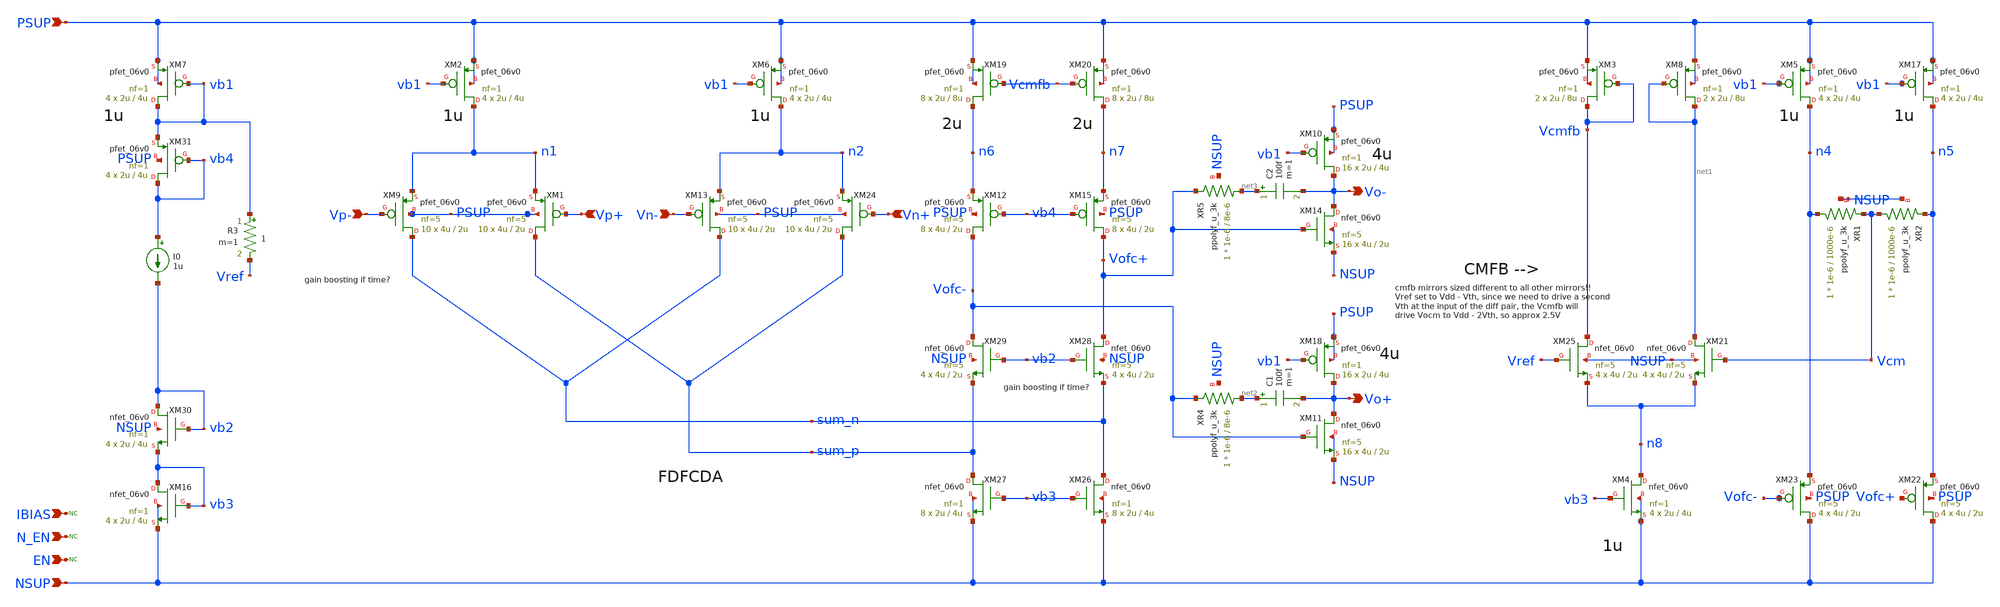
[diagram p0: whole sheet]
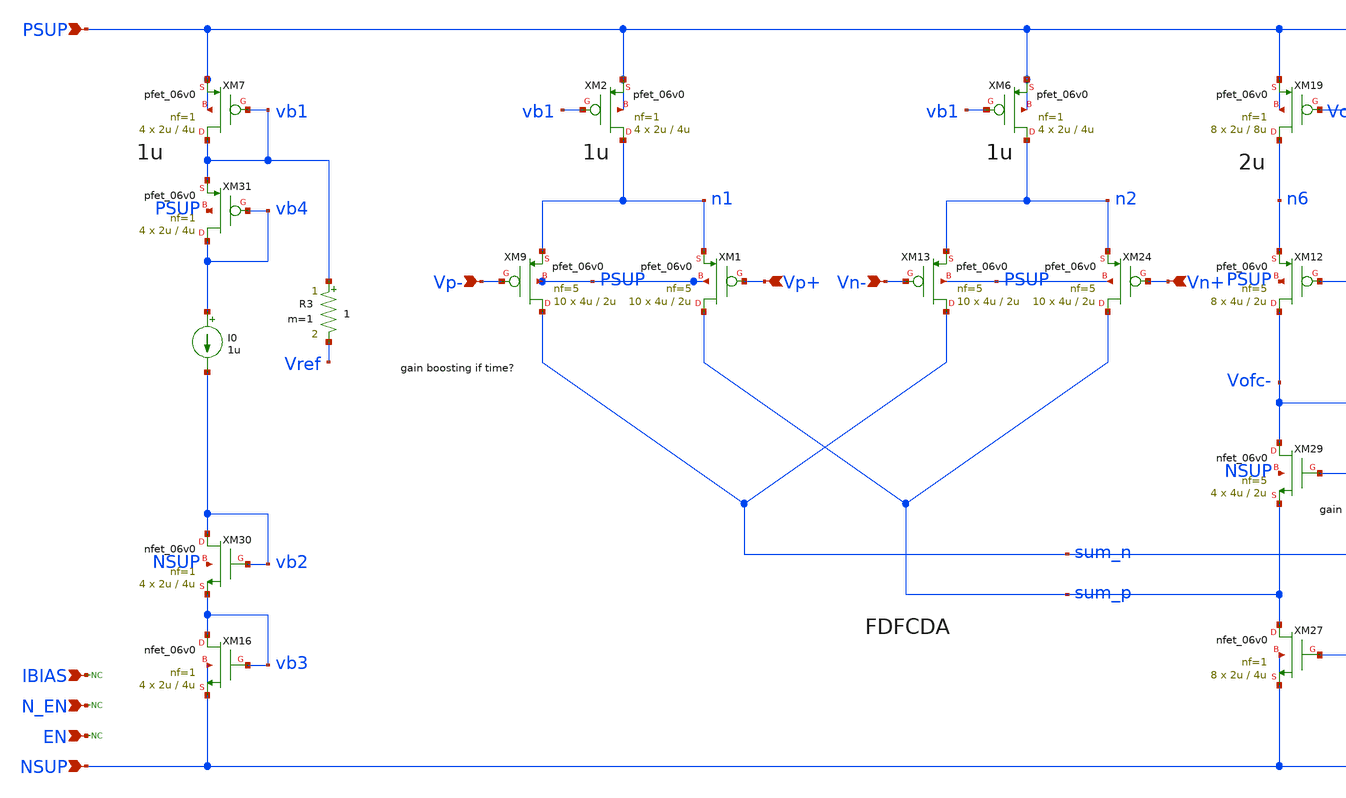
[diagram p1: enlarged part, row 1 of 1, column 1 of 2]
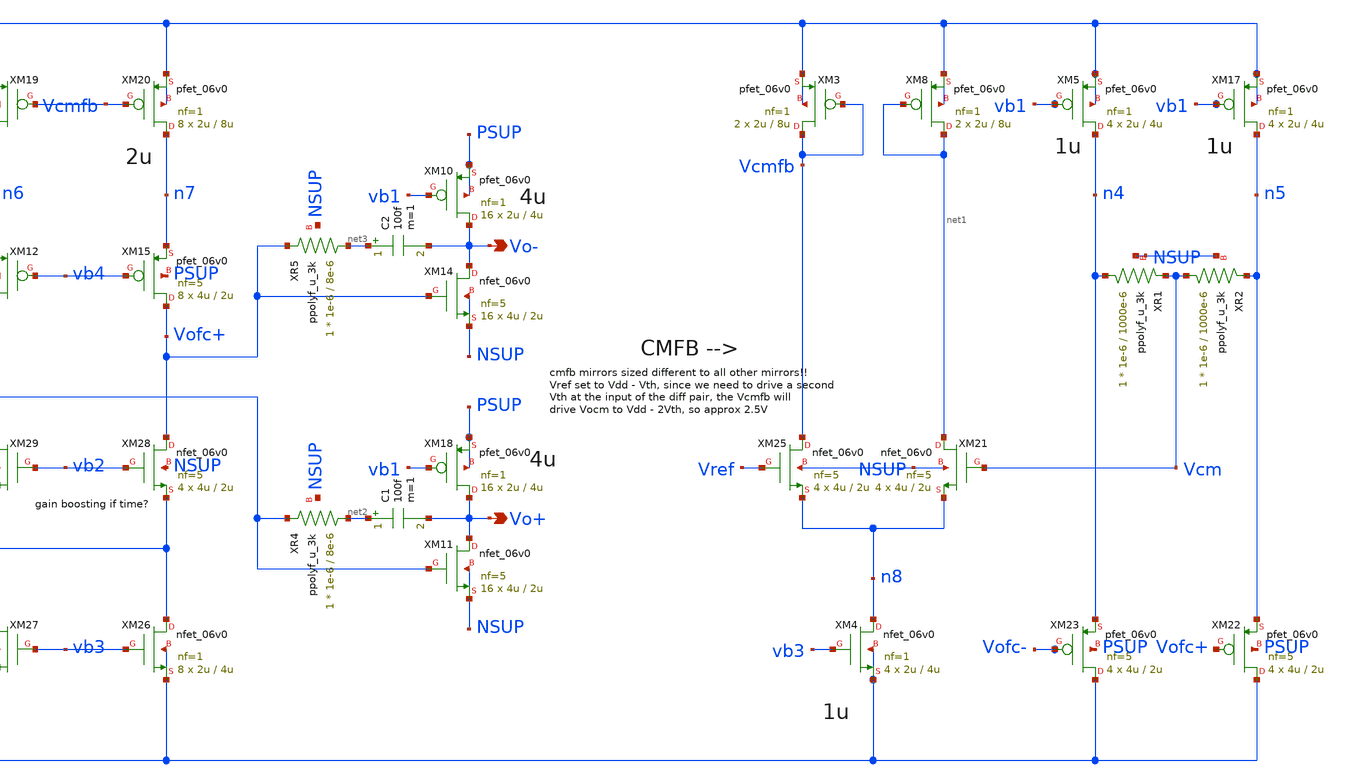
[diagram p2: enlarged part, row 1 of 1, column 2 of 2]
** sch_path: xschem/blocks/fdda/junk/fdda_most_recent.sch
**.subckt fdda_most_recent PSUP NSUP N_EN EN IBIAS Vp+ Vp- Vn+ Vn- Vo- Vo+
*.ipin PSUP
*.ipin NSUP
*.ipin N_EN
*.ipin EN
*.ipin IBIAS
*.ipin Vp+
*.ipin Vp-
*.ipin Vn+
*.ipin Vn-
*.opin Vo-
*.opin Vo+
* noconn N_EN
* noconn EN
I0 vb4 vb2 1u
XM7 vb1 vb1 PSUP PSUP pfet_06v0 L=4u W=2u nf=1 ad='int((nf+1)/2) * W/nf * 0.18u' as='int((nf+2)/2) * W/nf * 0.18u'
+ pd='2*int((nf+1)/2) * (W/nf + 0.18u)' ps='2*int((nf+2)/2) * (W/nf + 0.18u)' nrd='0.18u / W' nrs='0.18u / W'
+ sa=0 sb=0 sd=0 m=4
* noconn IBIAS
XM16 vb3 vb3 NSUP NSUP nfet_06v0 L=4u W=2u nf=1 ad='int((nf+1)/2) * W/nf * 0.18u' as='int((nf+2)/2) * W/nf * 0.18u'
+ pd='2*int((nf+1)/2) * (W/nf + 0.18u)' ps='2*int((nf+2)/2) * (W/nf + 0.18u)' nrd='0.18u / W' nrs='0.18u / W'
+ sa=0 sb=0 sd=0 m=4
XM9 sum_n Vp- n1 PSUP pfet_06v0 L=2u W=4u nf=5 ad='int((nf+1)/2) * W/nf * 0.18u' as='int((nf+2)/2) * W/nf * 0.18u'
+ pd='2*int((nf+1)/2) * (W/nf + 0.18u)' ps='2*int((nf+2)/2) * (W/nf + 0.18u)' nrd='0.18u / W' nrs='0.18u / W'
+ sa=0 sb=0 sd=0 m=10
XM1 sum_p Vp+ n1 PSUP pfet_06v0 L=2u W=4u nf=5 ad='int((nf+1)/2) * W/nf * 0.18u' as='int((nf+2)/2) * W/nf * 0.18u'
+ pd='2*int((nf+1)/2) * (W/nf + 0.18u)' ps='2*int((nf+2)/2) * (W/nf + 0.18u)' nrd='0.18u / W' nrs='0.18u / W'
+ sa=0 sb=0 sd=0 m=10
XM2 n1 vb1 PSUP PSUP pfet_06v0 L=4u W=2u nf=1 ad='int((nf+1)/2) * W/nf * 0.18u' as='int((nf+2)/2) * W/nf * 0.18u'
+ pd='2*int((nf+1)/2) * (W/nf + 0.18u)' ps='2*int((nf+2)/2) * (W/nf + 0.18u)' nrd='0.18u / W' nrs='0.18u / W'
+ sa=0 sb=0 sd=0 m=4
XM6 n2 vb1 PSUP PSUP pfet_06v0 L=4u W=2u nf=1 ad='int((nf+1)/2) * W/nf * 0.18u' as='int((nf+2)/2) * W/nf * 0.18u'
+ pd='2*int((nf+1)/2) * (W/nf + 0.18u)' ps='2*int((nf+2)/2) * (W/nf + 0.18u)' nrd='0.18u / W' nrs='0.18u / W'
+ sa=0 sb=0 sd=0 m=4
XM24 sum_p Vn+ n2 PSUP pfet_06v0 L=2u W=4u nf=5 ad='int((nf+1)/2) * W/nf * 0.18u' as='int((nf+2)/2) * W/nf * 0.18u'
+ pd='2*int((nf+1)/2) * (W/nf + 0.18u)' ps='2*int((nf+2)/2) * (W/nf + 0.18u)' nrd='0.18u / W' nrs='0.18u / W'
+ sa=0 sb=0 sd=0 m=10
XM13 sum_n Vn- n2 PSUP pfet_06v0 L=2u W=4u nf=5 ad='int((nf+1)/2) * W/nf * 0.18u' as='int((nf+2)/2) * W/nf * 0.18u'
+ pd='2*int((nf+1)/2) * (W/nf + 0.18u)' ps='2*int((nf+2)/2) * (W/nf + 0.18u)' nrd='0.18u / W' nrs='0.18u / W'
+ sa=0 sb=0 sd=0 m=10
XM12 Vofc- vb4 n6 PSUP pfet_06v0 L=2u W=4u nf=5 ad='int((nf+1)/2) * W/nf * 0.18u' as='int((nf+2)/2) * W/nf * 0.18u'
+ pd='2*int((nf+1)/2) * (W/nf + 0.18u)' ps='2*int((nf+2)/2) * (W/nf + 0.18u)' nrd='0.18u / W' nrs='0.18u / W'
+ sa=0 sb=0 sd=0 m=8
XM15 Vofc+ vb4 n7 PSUP pfet_06v0 L=2u W=4u nf=5 ad='int((nf+1)/2) * W/nf * 0.18u' as='int((nf+2)/2) * W/nf * 0.18u'
+ pd='2*int((nf+1)/2) * (W/nf + 0.18u)' ps='2*int((nf+2)/2) * (W/nf + 0.18u)' nrd='0.18u / W' nrs='0.18u / W'
+ sa=0 sb=0 sd=0 m=8
XM19 n6 Vcmfb PSUP PSUP pfet_06v0 L=8u W=2u nf=1 ad='int((nf+1)/2) * W/nf * 0.18u' as='int((nf+2)/2) * W/nf * 0.18u'
+ pd='2*int((nf+1)/2) * (W/nf + 0.18u)' ps='2*int((nf+2)/2) * (W/nf + 0.18u)' nrd='0.18u / W' nrs='0.18u / W'
+ sa=0 sb=0 sd=0 m=8
XM20 n7 Vcmfb PSUP PSUP pfet_06v0 L=8u W=2u nf=1 ad='int((nf+1)/2) * W/nf * 0.18u' as='int((nf+2)/2) * W/nf * 0.18u'
+ pd='2*int((nf+1)/2) * (W/nf + 0.18u)' ps='2*int((nf+2)/2) * (W/nf + 0.18u)' nrd='0.18u / W' nrs='0.18u / W'
+ sa=0 sb=0 sd=0 m=8
XM26 sum_n vb3 NSUP NSUP nfet_06v0 L=4u W=2u nf=1 ad='int((nf+1)/2) * W/nf * 0.18u' as='int((nf+2)/2) * W/nf * 0.18u'
+ pd='2*int((nf+1)/2) * (W/nf + 0.18u)' ps='2*int((nf+2)/2) * (W/nf + 0.18u)' nrd='0.18u / W' nrs='0.18u / W'
+ sa=0 sb=0 sd=0 m=8
XM27 sum_p vb3 NSUP NSUP nfet_06v0 L=4u W=2u nf=1 ad='int((nf+1)/2) * W/nf * 0.18u' as='int((nf+2)/2) * W/nf * 0.18u'
+ pd='2*int((nf+1)/2) * (W/nf + 0.18u)' ps='2*int((nf+2)/2) * (W/nf + 0.18u)' nrd='0.18u / W' nrs='0.18u / W'
+ sa=0 sb=0 sd=0 m=8
XM28 Vofc+ vb2 sum_n NSUP nfet_06v0 L=2u W=4u nf=5 ad='int((nf+1)/2) * W/nf * 0.18u' as='int((nf+2)/2) * W/nf * 0.18u'
+ pd='2*int((nf+1)/2) * (W/nf + 0.18u)' ps='2*int((nf+2)/2) * (W/nf + 0.18u)' nrd='0.18u / W' nrs='0.18u / W'
+ sa=0 sb=0 sd=0 m=4
XM29 Vofc- vb2 sum_p NSUP nfet_06v0 L=2u W=4u nf=5 ad='int((nf+1)/2) * W/nf * 0.18u' as='int((nf+2)/2) * W/nf * 0.18u'
+ pd='2*int((nf+1)/2) * (W/nf + 0.18u)' ps='2*int((nf+2)/2) * (W/nf + 0.18u)' nrd='0.18u / W' nrs='0.18u / W'
+ sa=0 sb=0 sd=0 m=4
XM30 vb2 vb2 vb3 NSUP nfet_06v0 L=4u W=2u nf=1 ad='int((nf+1)/2) * W/nf * 0.18u' as='int((nf+2)/2) * W/nf * 0.18u'
+ pd='2*int((nf+1)/2) * (W/nf + 0.18u)' ps='2*int((nf+2)/2) * (W/nf + 0.18u)' nrd='0.18u / W' nrs='0.18u / W'
+ sa=0 sb=0 sd=0 m=4
XM31 vb4 vb4 vb1 PSUP pfet_06v0 L=4u W=2u nf=1 ad='int((nf+1)/2) * W/nf * 0.18u' as='int((nf+2)/2) * W/nf * 0.18u'
+ pd='2*int((nf+1)/2) * (W/nf + 0.18u)' ps='2*int((nf+2)/2) * (W/nf + 0.18u)' nrd='0.18u / W' nrs='0.18u / W'
+ sa=0 sb=0 sd=0 m=4
XM3 Vcmfb Vcmfb PSUP PSUP pfet_06v0 L=8u W=2u nf=1 ad='int((nf+1)/2) * W/nf * 0.18u' as='int((nf+2)/2) * W/nf * 0.18u'
+ pd='2*int((nf+1)/2) * (W/nf + 0.18u)' ps='2*int((nf+2)/2) * (W/nf + 0.18u)' nrd='0.18u / W' nrs='0.18u / W'
+ sa=0 sb=0 sd=0 m=2
XM8 net1 net1 PSUP PSUP pfet_06v0 L=8u W=2u nf=1 ad='int((nf+1)/2) * W/nf * 0.18u' as='int((nf+2)/2) * W/nf * 0.18u'
+ pd='2*int((nf+1)/2) * (W/nf + 0.18u)' ps='2*int((nf+2)/2) * (W/nf + 0.18u)' nrd='0.18u / W' nrs='0.18u / W'
+ sa=0 sb=0 sd=0 m=2
XM21 net1 Vcm n8 NSUP nfet_06v0 L=2u W=4u nf=5 ad='int((nf+1)/2) * W/nf * 0.18u' as='int((nf+2)/2) * W/nf * 0.18u'
+ pd='2*int((nf+1)/2) * (W/nf + 0.18u)' ps='2*int((nf+2)/2) * (W/nf + 0.18u)' nrd='0.18u / W' nrs='0.18u / W'
+ sa=0 sb=0 sd=0 m=4
XM25 Vcmfb Vref n8 NSUP nfet_06v0 L=2u W=4u nf=5 ad='int((nf+1)/2) * W/nf * 0.18u' as='int((nf+2)/2) * W/nf * 0.18u'
+ pd='2*int((nf+1)/2) * (W/nf + 0.18u)' ps='2*int((nf+2)/2) * (W/nf + 0.18u)' nrd='0.18u / W' nrs='0.18u / W'
+ sa=0 sb=0 sd=0 m=4
XM4 n8 vb3 NSUP NSUP nfet_06v0 L=4u W=2u nf=1 ad='int((nf+1)/2) * W/nf * 0.18u' as='int((nf+2)/2) * W/nf * 0.18u'
+ pd='2*int((nf+1)/2) * (W/nf + 0.18u)' ps='2*int((nf+2)/2) * (W/nf + 0.18u)' nrd='0.18u / W' nrs='0.18u / W'
+ sa=0 sb=0 sd=0 m=4
XM22 NSUP Vofc+ n5 PSUP pfet_06v0 L=2u W=4u nf=5 ad='int((nf+1)/2) * W/nf * 0.18u' as='int((nf+2)/2) * W/nf * 0.18u'
+ pd='2*int((nf+1)/2) * (W/nf + 0.18u)' ps='2*int((nf+2)/2) * (W/nf + 0.18u)' nrd='0.18u / W' nrs='0.18u / W'
+ sa=0 sb=0 sd=0 m=4
XM23 NSUP Vofc- n4 PSUP pfet_06v0 L=2u W=4u nf=5 ad='int((nf+1)/2) * W/nf * 0.18u' as='int((nf+2)/2) * W/nf * 0.18u'
+ pd='2*int((nf+1)/2) * (W/nf + 0.18u)' ps='2*int((nf+2)/2) * (W/nf + 0.18u)' nrd='0.18u / W' nrs='0.18u / W'
+ sa=0 sb=0 sd=0 m=4
XR1 n4 Vcm NSUP ppolyf_u_3k r_width=1e-6 r_length=1000e-6 m=1
XR2 Vcm n5 NSUP ppolyf_u_3k r_width=1e-6 r_length=1000e-6 m=1
XM5 n4 vb1 PSUP PSUP pfet_06v0 L=4u W=2u nf=1 ad='int((nf+1)/2) * W/nf * 0.18u' as='int((nf+2)/2) * W/nf * 0.18u'
+ pd='2*int((nf+1)/2) * (W/nf + 0.18u)' ps='2*int((nf+2)/2) * (W/nf + 0.18u)' nrd='0.18u / W' nrs='0.18u / W'
+ sa=0 sb=0 sd=0 m=4
XM17 n5 vb1 PSUP PSUP pfet_06v0 L=4u W=2u nf=1 ad='int((nf+1)/2) * W/nf * 0.18u' as='int((nf+2)/2) * W/nf * 0.18u'
+ pd='2*int((nf+1)/2) * (W/nf + 0.18u)' ps='2*int((nf+2)/2) * (W/nf + 0.18u)' nrd='0.18u / W' nrs='0.18u / W'
+ sa=0 sb=0 sd=0 m=4
R3 vb1 Vref 1 m=1
XM14 Vo- Vofc+ NSUP NSUP nfet_06v0 L=2u W=4u nf=5 ad='int((nf+1)/2) * W/nf * 0.18u' as='int((nf+2)/2) * W/nf * 0.18u'
+ pd='2*int((nf+1)/2) * (W/nf + 0.18u)' ps='2*int((nf+2)/2) * (W/nf + 0.18u)' nrd='0.18u / W' nrs='0.18u / W'
+ sa=0 sb=0 sd=0 m=16
XM10 Vo- vb1 PSUP PSUP pfet_06v0 L=4u W=2u nf=1 ad='int((nf+1)/2) * W/nf * 0.18u' as='int((nf+2)/2) * W/nf * 0.18u'
+ pd='2*int((nf+1)/2) * (W/nf + 0.18u)' ps='2*int((nf+2)/2) * (W/nf + 0.18u)' nrd='0.18u / W' nrs='0.18u / W'
+ sa=0 sb=0 sd=0 m=16
XM11 Vo+ Vofc- NSUP NSUP nfet_06v0 L=2u W=4u nf=5 ad='int((nf+1)/2) * W/nf * 0.18u' as='int((nf+2)/2) * W/nf * 0.18u'
+ pd='2*int((nf+1)/2) * (W/nf + 0.18u)' ps='2*int((nf+2)/2) * (W/nf + 0.18u)' nrd='0.18u / W' nrs='0.18u / W'
+ sa=0 sb=0 sd=0 m=16
XM18 Vo+ vb1 PSUP PSUP pfet_06v0 L=4u W=2u nf=1 ad='int((nf+1)/2) * W/nf * 0.18u' as='int((nf+2)/2) * W/nf * 0.18u'
+ pd='2*int((nf+1)/2) * (W/nf + 0.18u)' ps='2*int((nf+2)/2) * (W/nf + 0.18u)' nrd='0.18u / W' nrs='0.18u / W'
+ sa=0 sb=0 sd=0 m=16
C1 net2 Vo+ 100f m=1
XR4 net2 Vofc- NSUP ppolyf_u_3k r_width=1e-6 r_length=8e-6 m=1
C2 net3 Vo- 100f m=1
XR5 net3 Vofc+ NSUP ppolyf_u_3k r_width=1e-6 r_length=8e-6 m=1
**.ends
.end
